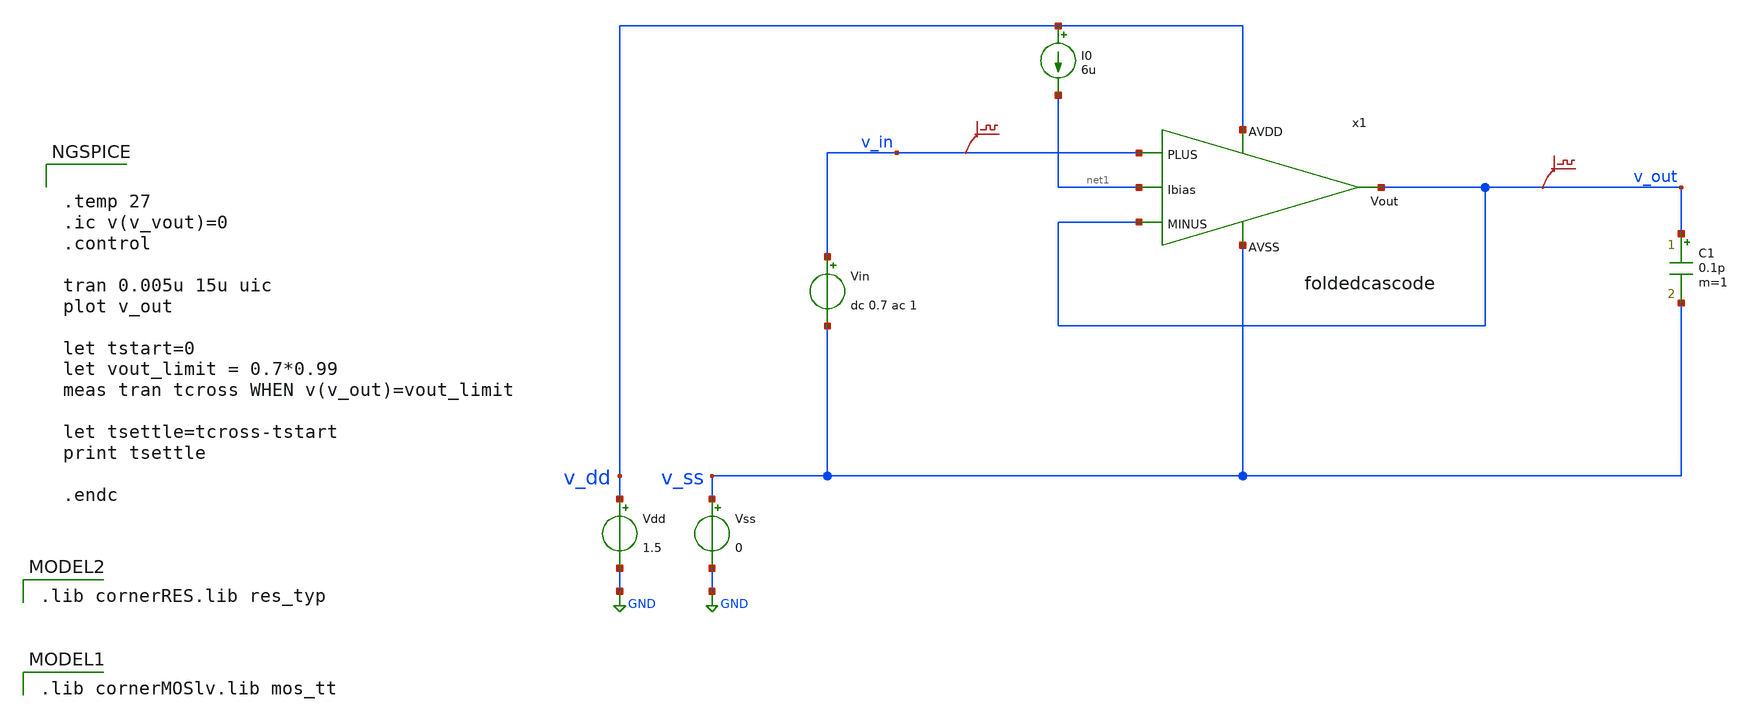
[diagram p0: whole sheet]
** sch_path: Designs/otas/tb_foldedcascode_tran.sch
* (c) 2024 Hrishikesh, @HSB
* Designs/otas/foldedcascode.sch:
* (c) 2025 Thesis_HP, Apache-2.0 license
**.subckt tb_foldedcascode_tran
Vdd v_dd GND 1.5
Vss v_ss GND 0
C1 v_out v_ss 0.1p m=1
Vin v_in v_ss dc 0.7 ac 1
I0 v_dd net1 6u
.save v(v_in)
.save v(v_out)
x1 v_dd net1 v_in v_out v_out v_ss foldedcascode
**** begin user architecture code
 .lib cornerMOSlv.lib mos_tt

 .lib cornerRES.lib res_typ



.temp 27
.ic v(v_vout)=0
.control

tran 0.005u 15u uic
plot v_out

let tstart=0
let vout_limit = 0.7*0.99
meas tran tcross WHEN v(v_out)=vout_limit

let tsettle=tcross-tstart
print tsettle

.endc


**** end user architecture code
**.ends

* expanding   symbol:  foldedcascode.sym # of pins=6
** sym_path: Designs/otas/foldedcascode.sym
** sch_path: Designs/otas/foldedcascode.sch
.subckt foldedcascode AVDD Ibias PLUS MINUS Vout AVSS
*.ipin AVDD
*.ipin AVSS
*.ipin PLUS
*.ipin MINUS
*.opin Vout
*.ipin Ibias
XMt2 net1 Ibias AVDD AVDD sg13_lv_pmos w=21u l=1u ng=3 m=1 mm_ok=1
XM1 net3 PLUS net1 AVDD sg13_lv_pmos w=19.5u l=1u ng=2 m=1 mm_ok=1
XM2 net8 MINUS net1 AVDD sg13_lv_pmos w=19.5u l=1u ng=2 m=1 mm_ok=1
XM6 net6 Vout AVDD AVDD sg13_lv_pmos w=3u l=0.5u ng=1 m=1 mm_ok=1
XM7 net5 net4 net6 AVDD sg13_lv_pmos w=5u l=0.5u ng=2 m=1 mm_ok=1
XM8 net7 Vout AVDD AVDD sg13_lv_pmos w=3u l=0.5u ng=1 m=1 mm_ok=1
XM15 Vout net4 net7 AVDD sg13_lv_pmos w=5u l=0.5u ng=2 m=1 mm_ok=1
XM16 Vout Ibias net8 AVSS sg13_lv_nmos w=1.5u l=0.5u ng=1 m=1 mm_ok=1
XM17 net8 net2 AVSS AVSS sg13_lv_nmos w=1.5u l=0.5u ng=1 m=1 mm_ok=1
XM18 net5 Ibias net3 AVSS sg13_lv_nmos w=1.5u l=0.5u ng=1 m=1 mm_ok=1
XM27 net3 net2 AVSS AVSS sg13_lv_nmos w=1.5u l=0.5u ng=1 m=1 mm_ok=1
XM28 Ibias Ibias AVDD AVDD sg13_lv_pmos w=15u l=1u ng=3 m=1 mm_ok=1
XM29 Ibias Ibias net2 AVSS sg13_lv_nmos w=3u l=0.5u ng=1 m=1 mm_ok=1
XM30 net2 net2 AVSS AVSS sg13_lv_nmos w=3u l=0.5u ng=1 m=1 mm_ok=1
XM31 AVDD Ibias net9 AVSS sg13_lv_nmos w=3u l=0.5u ng=1 m=1 mm_ok=1
XM32 net9 net2 AVSS AVSS sg13_lv_nmos w=3u l=0.5u ng=1 m=1 mm_ok=1
XM33 net4 net2 AVSS AVSS sg13_lv_nmos w=3u l=0.5u ng=1 m=1 mm_ok=1
XM34 net4 net4 AVDD AVDD sg13_lv_pmos w=10u l=0.5u ng=2 m=1 mm_ok=1
XMdecoup1 AVDD net4 AVDD AVDD sg13_lv_pmos w=12u l=0.5u ng=4 m=1 mm_ok=1
XMdecoup2 AVDD Ibias AVDD AVDD sg13_lv_pmos w=12u l=0.5u ng=4 m=1 mm_ok=1
XMdecoup3 AVSS Ibias AVSS AVSS sg13_lv_nmos w=8u l=1u ng=4 m=1 mm_ok=1
XMdecoup4 AVSS net2 AVSS AVSS sg13_lv_nmos w=8u l=1u ng=4 m=1 mm_ok=1
XMdecoup5 AVSS net2 AVSS AVSS sg13_lv_nmos w=8u l=1u ng=4 m=1 mm_ok=1
.ends

.GLOBAL GND
.end
